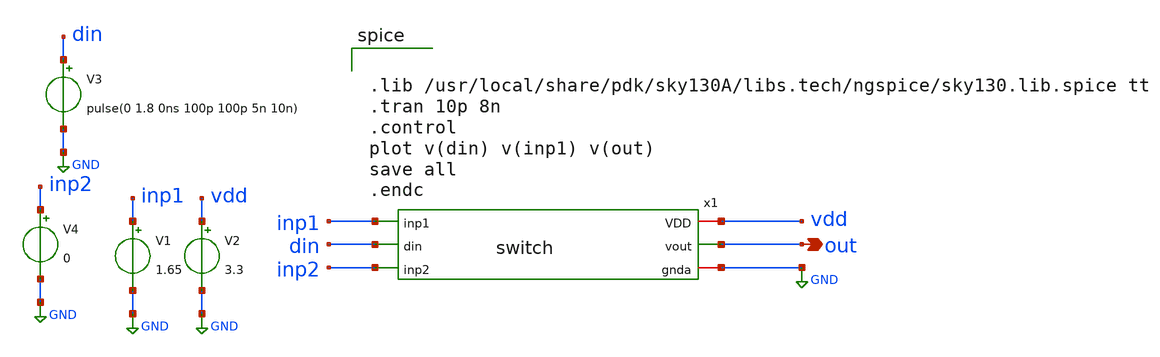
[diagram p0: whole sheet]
** sch_path: week7/pre-layout/untitled-1.sch
**.subckt untitled-1 out
*.opin out
x1 inp1 vdd din out GND inp2 switch
V1 inp1 GND 1.65
V2 vdd GND 3.3
V3 din GND pulse(0 1.8 0ns 100p 100p 5n 10n)
V4 inp2 GND 0
**** begin user architecture code


.lib /usr/local/share/pdk/sky130A/libs.tech/ngspice/sky130.lib.spice tt
.tran 10p 8n
.control
plot v(din) v(inp1) v(out)
save all
.endc


**** end user architecture code
**.ends

* expanding   symbol:  switch.sym # of pins=6
** sym_path: week7/pre-layout/switch.sym
** sch_path: week7/pre-layout/switch.sch
.subckt switch inp1 VDD din vout gnda inp2
*.ipin din
*.iopin VDD
*.ipin inp1
*.ipin inp2
*.iopin gnda
*.opin vout
XM1 net1 din gnda gnda sky130_fd_pr__nfet_01v8 L=0.15 W=0.6 nf=1 ad='int((nf+1)/2) * W/nf * 0.29' as='int((nf+2)/2) * W/nf * 0.29'
+ pd='2*int((nf+1)/2) * (W/nf + 0.29)' ps='2*int((nf+2)/2) * (W/nf + 0.29)' nrd='0.29 / W' nrs='0.29 / W'
+ sa=0 sb=0 sd=0 mult=1 m=1
XM2 net1 din VDD VDD sky130_fd_pr__pfet_01v8 L=0.15 W=1.2 nf=1 ad='int((nf+1)/2) * W/nf * 0.29' as='int((nf+2)/2) * W/nf * 0.29'
+ pd='2*int((nf+1)/2) * (W/nf + 0.29)' ps='2*int((nf+2)/2) * (W/nf + 0.29)' nrd='0.29 / W' nrs='0.29 / W'
+ sa=0 sb=0 sd=0 mult=1 m=1
XM3 net2 net1 VDD VDD sky130_fd_pr__pfet_01v8 L=0.15 W=1.2 nf=1 ad='int((nf+1)/2) * W/nf * 0.29' as='int((nf+2)/2) * W/nf * 0.29'
+ pd='2*int((nf+1)/2) * (W/nf + 0.29)' ps='2*int((nf+2)/2) * (W/nf + 0.29)' nrd='0.29 / W' nrs='0.29 / W'
+ sa=0 sb=0 sd=0 mult=1 m=1
XM4 net2 net1 gnda gnda sky130_fd_pr__nfet_01v8 L=0.15 W=0.6 nf=1 ad='int((nf+1)/2) * W/nf * 0.29' as='int((nf+2)/2) * W/nf * 0.29'
+ pd='2*int((nf+1)/2) * (W/nf + 0.29)' ps='2*int((nf+2)/2) * (W/nf + 0.29)' nrd='0.29 / W' nrs='0.29 / W'
+ sa=0 sb=0 sd=0 mult=1 m=1
XM5 inp2 net2 vout VDD sky130_fd_pr__pfet_01v8 L=0.15 W=1.2 nf=1 ad='int((nf+1)/2) * W/nf * 0.29' as='int((nf+2)/2) * W/nf * 0.29'
+ pd='2*int((nf+1)/2) * (W/nf + 0.29)' ps='2*int((nf+2)/2) * (W/nf + 0.29)' nrd='0.29 / W' nrs='0.29 / W'
+ sa=0 sb=0 sd=0 mult=1 m=1
XM6 inp1 net2 vout GND sky130_fd_pr__nfet_01v8 L=0.15 W=0.6 nf=1 ad='int((nf+1)/2) * W/nf * 0.29' as='int((nf+2)/2) * W/nf * 0.29'
+ pd='2*int((nf+1)/2) * (W/nf + 0.29)' ps='2*int((nf+2)/2) * (W/nf + 0.29)' nrd='0.29 / W' nrs='0.29 / W'
+ sa=0 sb=0 sd=0 mult=1 m=1
XM7 vout net1 inp2 GND sky130_fd_pr__nfet_01v8 L=0.15 W=0.6 nf=1 ad='int((nf+1)/2) * W/nf * 0.29' as='int((nf+2)/2) * W/nf * 0.29'
+ pd='2*int((nf+1)/2) * (W/nf + 0.29)' ps='2*int((nf+2)/2) * (W/nf + 0.29)' nrd='0.29 / W' nrs='0.29 / W'
+ sa=0 sb=0 sd=0 mult=1 m=1
XM8 vout net1 inp1 VDD sky130_fd_pr__pfet_01v8 L=0.15 W=1.2 nf=1 ad='int((nf+1)/2) * W/nf * 0.29' as='int((nf+2)/2) * W/nf * 0.29'
+ pd='2*int((nf+1)/2) * (W/nf + 0.29)' ps='2*int((nf+2)/2) * (W/nf + 0.29)' nrd='0.29 / W' nrs='0.29 / W'
+ sa=0 sb=0 sd=0 mult=1 m=1
.ends

.GLOBAL GND
.end
